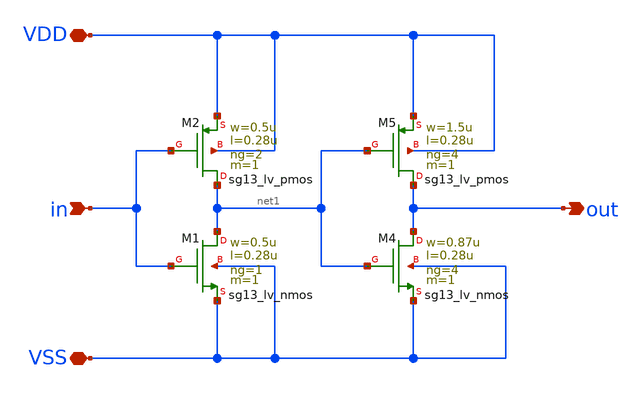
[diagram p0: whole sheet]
** sch_path: blocks/composite/dpi_adexp_neuron/design_data/xschem/buff.sch
**.subckt buff VDD in VSS out
*.iopin VDD
*.ipin in
*.iopin VSS
*.opin out
XM1 net1 in VSS VSS sg13_lv_nmos w=0.5u l=0.28u ng=1 m=1 mm_ok=1
XM2 net1 in VDD VDD sg13_lv_pmos w=0.5u l=0.28u ng=2 m=1 mm_ok=1
XM4 out net1 VSS VSS sg13_lv_nmos w=0.87u l=0.28u ng=4 m=1 mm_ok=1
XM5 out net1 VDD VDD sg13_lv_pmos w=1.5u l=0.28u ng=4 m=1 mm_ok=1
**.ends
.end
